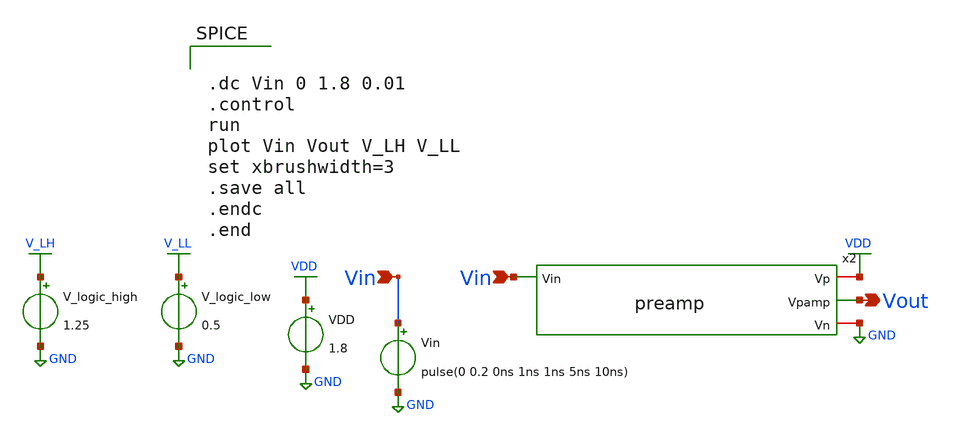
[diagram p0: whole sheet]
** sch_path: xschem/Vth_sch/Pre_layout/preamp.sch
**.subckt preamp Vin Vout Vin
*.ipin Vin
*.opin Vout
*.ipin Vin
VDD VDD GND 1.8
Vin Vin GND pulse(0 0.2 0ns 1ns 1ns 5ns 10ns)
V_logic_high V_LH GND 1.25
V_logic_low V_LL GND 0.5
x2 VDD Vin Vout GND preamp
**** begin user architecture code


.lib /usr/local/share/pdk/sky130A/libs.tech/ngspice/sky130.lib.spice tt

.save all





.dc Vin 0 1.8 0.01
.control
run
plot Vin Vout V_LH V_LL
set xbrushwidth=3
.save all
.endc
.end


**** end user architecture code
**.ends

* expanding   symbol:  /home/exotic/Desktop/ASIC_ADC/xschem/Vth_sch/Symbol/preamp.sym # of pins=4
** sym_path: xschem/Vth_sch/Symbol/preamp.sym
** sch_path: xschem/Vth_sch/Symbol/preamp.sch
.subckt preamp Vp Vin Vpamp Vn
*.ipin Vin
*.opin Vpamp
*.iopin Vp
*.iopin Vn
XM1 Vp Vin Vpamp Vn sky130_fd_pr__nfet_01v8 L=3.5 W=1 nf=1 ad='int((nf+1)/2) * W/nf * 0.29' as='int((nf+2)/2) * W/nf * 0.29'
+ pd='2*int((nf+1)/2) * (W/nf + 0.29)' ps='2*int((nf+2)/2) * (W/nf + 0.29)' nrd='0.29 / W' nrs='0.29 / W'
+ sa=0 sb=0 sd=0 mult=1 m=1
XM0 Vn Vin Vpamp Vp sky130_fd_pr__pfet_01v8 L=0.150 W=0.63 nf=1 ad='int((nf+1)/2) * W/nf * 0.29' as='int((nf+2)/2) * W/nf * 0.29'
+ pd='2*int((nf+1)/2) * (W/nf + 0.29)' ps='2*int((nf+2)/2) * (W/nf + 0.29)' nrd='0.29 / W' nrs='0.29 / W'
+ sa=0 sb=0 sd=0 mult=1 m=1
.ends

.GLOBAL VDD
.GLOBAL GND
.GLOBAL V_LH
.GLOBAL V_LL
.end
